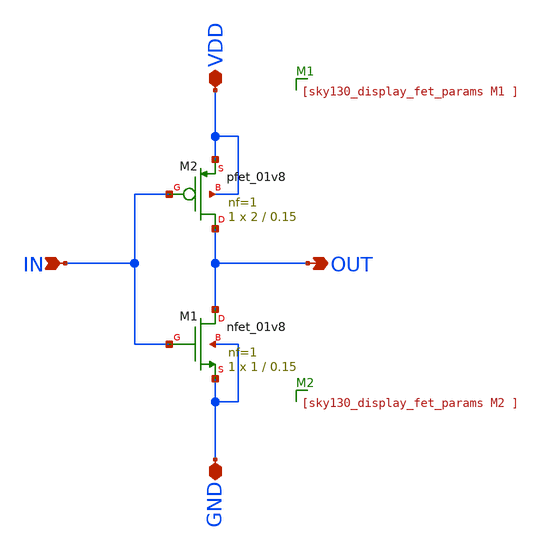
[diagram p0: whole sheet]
** sch_path: 01_xschem_ngspice/soluzioni/lab01/xschem/inverter.sch
**.subckt inverter IN OUT VDD GND
*.ipin IN
*.opin OUT
*.iopin VDD
*.iopin GND
XM1 OUT IN GND GND sky130_fd_pr__nfet_01v8 L=0.15 W=1 nf=1 ad='int((1 + 1)/2) * 1 / 1 * 0.29' as='int((1 + 2)/2) * 1 / 1 * 0.29'
+ pd='2*int((1 + 1)/2) * (1 / 1 + 0.29)' ps='2*int((1 + 2)/2) * (1 / 1 + 0.29)' nrd='0.29 / 1 ' nrs='0.29 / 1 '
+ sa=0 sb=0 sd=0 mult=1 m=1
XM2 OUT IN VDD VDD sky130_fd_pr__pfet_01v8 L=0.15 W=2 nf=1 ad='int((1 + 1)/2) * 2 / 1 * 0.29' as='int((1 + 2)/2) * 2 / 1 * 0.29'
+ pd='2*int((1 + 1)/2) * (2 / 1 + 0.29)' ps='2*int((1 + 2)/2) * (2 / 1 + 0.29)' nrd='0.29 / 2 ' nrs='0.29 / 2 '
+ sa=0 sb=0 sd=0 mult=1 m=1
**.ends
.end
